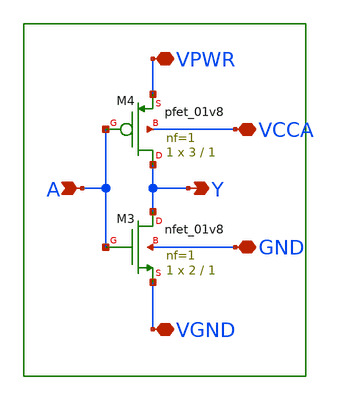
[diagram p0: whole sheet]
** sch_path: xschem/lib_dco/dco_aux_inv.sch
**.subckt dco_aux_inv VPWR VGND A Y VCCA GND
*.iopin VPWR
*.iopin VGND
*.ipin A
*.opin Y
*.iopin VCCA
*.iopin GND
XM3 Y A VGND GND sky130_fd_pr__nfet_01v8 L=1 W=2 nf=1 ad='int((nf+1)/2) * W/nf * 0.29' as='int((nf+2)/2) * W/nf * 0.29'
+ pd='2*int((nf+1)/2) * (W/nf + 0.29)' ps='2*int((nf+2)/2) * (W/nf + 0.29)' nrd='0.29 / W' nrs='0.29 / W'
+ sa=0 sb=0 sd=0 mult=1 m=1
XM4 Y A VPWR VCCA sky130_fd_pr__pfet_01v8 L=1 W=3 nf=1 ad='int((nf+1)/2) * W/nf * 0.29' as='int((nf+2)/2) * W/nf * 0.29'
+ pd='2*int((nf+1)/2) * (W/nf + 0.29)' ps='2*int((nf+2)/2) * (W/nf + 0.29)' nrd='0.29 / W' nrs='0.29 / W'
+ sa=0 sb=0 sd=0 mult=1 m=1
**.ends
.end
